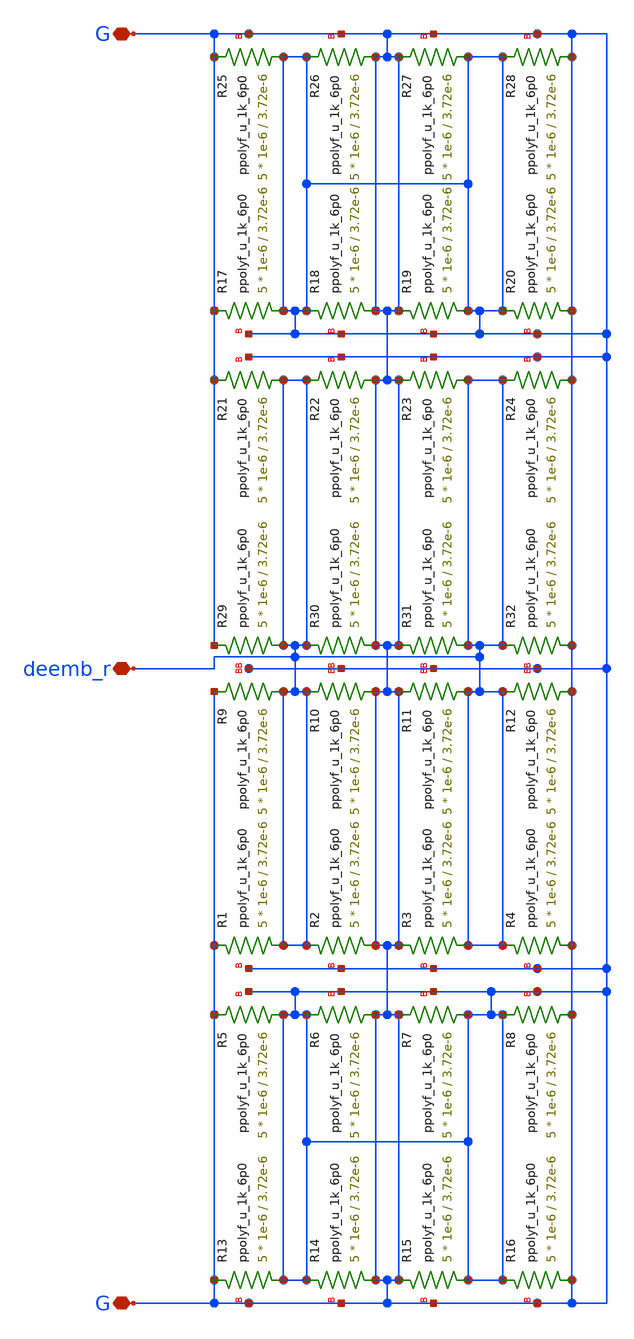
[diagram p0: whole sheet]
** sch_path: xschem/DEEMB_R.sch
**.subckt DEEMB_R G deemb_r G
*.iopin G
*.iopin deemb_r
*.iopin G
XR1 deemb_r G G ppolyf_u_1k_6p0 r_width=1e-6 r_length=3.72e-6 m=5
XR2 G deemb_r G ppolyf_u_1k_6p0 r_width=1e-6 r_length=3.72e-6 m=5
XR3 deemb_r G G ppolyf_u_1k_6p0 r_width=1e-6 r_length=3.72e-6 m=5
XR4 G deemb_r G ppolyf_u_1k_6p0 r_width=1e-6 r_length=3.72e-6 m=5
XR5 G G G ppolyf_u_1k_6p0 r_width=1e-6 r_length=3.72e-6 m=5
XR6 G G G ppolyf_u_1k_6p0 r_width=1e-6 r_length=3.72e-6 m=5
XR7 G G G ppolyf_u_1k_6p0 r_width=1e-6 r_length=3.72e-6 m=5
XR8 G G G ppolyf_u_1k_6p0 r_width=1e-6 r_length=3.72e-6 m=5
XR9 deemb_r G G ppolyf_u_1k_6p0 r_width=1e-6 r_length=3.72e-6 m=5
XR10 G deemb_r G ppolyf_u_1k_6p0 r_width=1e-6 r_length=3.72e-6 m=5
XR11 deemb_r G G ppolyf_u_1k_6p0 r_width=1e-6 r_length=3.72e-6 m=5
XR12 G deemb_r G ppolyf_u_1k_6p0 r_width=1e-6 r_length=3.72e-6 m=5
XR13 G G G ppolyf_u_1k_6p0 r_width=1e-6 r_length=3.72e-6 m=5
XR14 G G G ppolyf_u_1k_6p0 r_width=1e-6 r_length=3.72e-6 m=5
XR15 G G G ppolyf_u_1k_6p0 r_width=1e-6 r_length=3.72e-6 m=5
XR16 G G G ppolyf_u_1k_6p0 r_width=1e-6 r_length=3.72e-6 m=5
XR17 G G G ppolyf_u_1k_6p0 r_width=1e-6 r_length=3.72e-6 m=5
XR18 G G G ppolyf_u_1k_6p0 r_width=1e-6 r_length=3.72e-6 m=5
XR19 G G G ppolyf_u_1k_6p0 r_width=1e-6 r_length=3.72e-6 m=5
XR20 G G G ppolyf_u_1k_6p0 r_width=1e-6 r_length=3.72e-6 m=5
XR21 deemb_r G G ppolyf_u_1k_6p0 r_width=1e-6 r_length=3.72e-6 m=5
XR22 G deemb_r G ppolyf_u_1k_6p0 r_width=1e-6 r_length=3.72e-6 m=5
XR23 deemb_r G G ppolyf_u_1k_6p0 r_width=1e-6 r_length=3.72e-6 m=5
XR24 G deemb_r G ppolyf_u_1k_6p0 r_width=1e-6 r_length=3.72e-6 m=5
XR25 G G G ppolyf_u_1k_6p0 r_width=1e-6 r_length=3.72e-6 m=5
XR26 G G G ppolyf_u_1k_6p0 r_width=1e-6 r_length=3.72e-6 m=5
XR27 G G G ppolyf_u_1k_6p0 r_width=1e-6 r_length=3.72e-6 m=5
XR28 G G G ppolyf_u_1k_6p0 r_width=1e-6 r_length=3.72e-6 m=5
XR29 deemb_r G G ppolyf_u_1k_6p0 r_width=1e-6 r_length=3.72e-6 m=5
XR30 G deemb_r G ppolyf_u_1k_6p0 r_width=1e-6 r_length=3.72e-6 m=5
XR31 deemb_r G G ppolyf_u_1k_6p0 r_width=1e-6 r_length=3.72e-6 m=5
XR32 G deemb_r G ppolyf_u_1k_6p0 r_width=1e-6 r_length=3.72e-6 m=5
**.ends
.end
